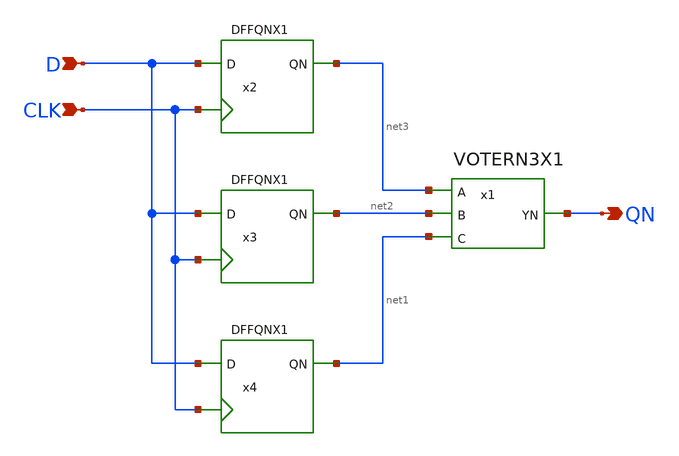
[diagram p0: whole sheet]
** sch_path: lib/xschem/TMRDFFQNX1.sch
**.subckt TMRDFFQNX1 D CLK QN
*.ipin D
*.ipin CLK
*.opin QN
x1 net3 net2 net1 QN VDD VSS VOTERN3X1
x2 CLK net3 D VDD VSS DFFQNX1
x3 CLK net2 D VDD VSS DFFQNX1
x4 CLK net1 D VDD VSS DFFQNX1
**.ends

* expanding   symbol:  VOTERN3X1.sym # of pins=4
** sym_path: VOTERN3X1.sym
** sch_path: VOTERN3X1.sch
.subckt VOTERN3X1 A B C YN VDD VSS
*.ipin A
*.opin YN
*.ipin B
*.ipin C
XM2 net1 A VDD VDD sky130_fd_pr__pfet_01v8 L=0.15 W=2 nf=1 ad='int((nf+1)/2) * W/nf * 0.29' as='int((nf+2)/2) * W/nf * 0.29'
+ pd='2*int((nf+1)/2) * (W/nf + 0.29)' ps='2*int((nf+2)/2) * (W/nf + 0.29)' nrd='0.29 / W' nrs='0.29 / W'
+ sa=0 sb=0 sd=0 mult=1 m=1
XM3 net2 B VSS VSS sky130_fd_pr__nfet_01v8 L=0.15 W=3 nf=1 ad='int((nf+1)/2) * W/nf * 0.29' as='int((nf+2)/2) * W/nf * 0.29'
+ pd='2*int((nf+1)/2) * (W/nf + 0.29)' ps='2*int((nf+2)/2) * (W/nf + 0.29)' nrd='0.29 / W' nrs='0.29 / W'
+ sa=0 sb=0 sd=0 mult=1 m=1
XM4 YN A net2 VSS sky130_fd_pr__nfet_01v8 L=0.15 W=3 nf=1 ad='int((nf+1)/2) * W/nf * 0.29' as='int((nf+2)/2) * W/nf * 0.29'
+ pd='2*int((nf+1)/2) * (W/nf + 0.29)' ps='2*int((nf+2)/2) * (W/nf + 0.29)' nrd='0.29 / W' nrs='0.29 / W'
+ sa=0 sb=0 sd=0 mult=1 m=1
XM5 net1 A VDD VDD sky130_fd_pr__pfet_01v8 L=0.15 W=2 nf=1 ad='int((nf+1)/2) * W/nf * 0.29' as='int((nf+2)/2) * W/nf * 0.29'
+ pd='2*int((nf+1)/2) * (W/nf + 0.29)' ps='2*int((nf+2)/2) * (W/nf + 0.29)' nrd='0.29 / W' nrs='0.29 / W'
+ sa=0 sb=0 sd=0 mult=1 m=1
XM6 net1 B VDD VDD sky130_fd_pr__pfet_01v8 L=0.15 W=2 nf=1 ad='int((nf+1)/2) * W/nf * 0.29' as='int((nf+2)/2) * W/nf * 0.29'
+ pd='2*int((nf+1)/2) * (W/nf + 0.29)' ps='2*int((nf+2)/2) * (W/nf + 0.29)' nrd='0.29 / W' nrs='0.29 / W'
+ sa=0 sb=0 sd=0 mult=1 m=1
XM7 net1 B VDD VDD sky130_fd_pr__pfet_01v8 L=0.15 W=2 nf=1 ad='int((nf+1)/2) * W/nf * 0.29' as='int((nf+2)/2) * W/nf * 0.29'
+ pd='2*int((nf+1)/2) * (W/nf + 0.29)' ps='2*int((nf+2)/2) * (W/nf + 0.29)' nrd='0.29 / W' nrs='0.29 / W'
+ sa=0 sb=0 sd=0 mult=1 m=1
XM10 net3 B net1 net1 sky130_fd_pr__pfet_01v8 L=0.15 W=2 nf=1 ad='int((nf+1)/2) * W/nf * 0.29' as='int((nf+2)/2) * W/nf * 0.29'
+ pd='2*int((nf+1)/2) * (W/nf + 0.29)' ps='2*int((nf+2)/2) * (W/nf + 0.29)' nrd='0.29 / W' nrs='0.29 / W'
+ sa=0 sb=0 sd=0 mult=1 m=1
XM11 net3 B net1 VDD sky130_fd_pr__pfet_01v8 L=0.15 W=2 nf=1 ad='int((nf+1)/2) * W/nf * 0.29' as='int((nf+2)/2) * W/nf * 0.29'
+ pd='2*int((nf+1)/2) * (W/nf + 0.29)' ps='2*int((nf+2)/2) * (W/nf + 0.29)' nrd='0.29 / W' nrs='0.29 / W'
+ sa=0 sb=0 sd=0 mult=1 m=1
XM12 YN C net3 net3 sky130_fd_pr__pfet_01v8 L=0.15 W=2 nf=1 ad='int((nf+1)/2) * W/nf * 0.29' as='int((nf+2)/2) * W/nf * 0.29'
+ pd='2*int((nf+1)/2) * (W/nf + 0.29)' ps='2*int((nf+2)/2) * (W/nf + 0.29)' nrd='0.29 / W' nrs='0.29 / W'
+ sa=0 sb=0 sd=0 mult=1 m=1
XM13 YN C net3 VDD sky130_fd_pr__pfet_01v8 L=0.15 W=2 nf=1 ad='int((nf+1)/2) * W/nf * 0.29' as='int((nf+2)/2) * W/nf * 0.29'
+ pd='2*int((nf+1)/2) * (W/nf + 0.29)' ps='2*int((nf+2)/2) * (W/nf + 0.29)' nrd='0.29 / W' nrs='0.29 / W'
+ sa=0 sb=0 sd=0 mult=1 m=1
XM14 net3 C net1 net1 sky130_fd_pr__pfet_01v8 L=0.15 W=2 nf=1 ad='int((nf+1)/2) * W/nf * 0.29' as='int((nf+2)/2) * W/nf * 0.29'
+ pd='2*int((nf+1)/2) * (W/nf + 0.29)' ps='2*int((nf+2)/2) * (W/nf + 0.29)' nrd='0.29 / W' nrs='0.29 / W'
+ sa=0 sb=0 sd=0 mult=1 m=1
XM15 net3 C net1 VDD sky130_fd_pr__pfet_01v8 L=0.15 W=2 nf=1 ad='int((nf+1)/2) * W/nf * 0.29' as='int((nf+2)/2) * W/nf * 0.29'
+ pd='2*int((nf+1)/2) * (W/nf + 0.29)' ps='2*int((nf+2)/2) * (W/nf + 0.29)' nrd='0.29 / W' nrs='0.29 / W'
+ sa=0 sb=0 sd=0 mult=1 m=1
XM16 YN A net3 net3 sky130_fd_pr__pfet_01v8 L=0.15 W=2 nf=1 ad='int((nf+1)/2) * W/nf * 0.29' as='int((nf+2)/2) * W/nf * 0.29'
+ pd='2*int((nf+1)/2) * (W/nf + 0.29)' ps='2*int((nf+2)/2) * (W/nf + 0.29)' nrd='0.29 / W' nrs='0.29 / W'
+ sa=0 sb=0 sd=0 mult=1 m=1
XM17 YN A net3 VDD sky130_fd_pr__pfet_01v8 L=0.15 W=2 nf=1 ad='int((nf+1)/2) * W/nf * 0.29' as='int((nf+2)/2) * W/nf * 0.29'
+ pd='2*int((nf+1)/2) * (W/nf + 0.29)' ps='2*int((nf+2)/2) * (W/nf + 0.29)' nrd='0.29 / W' nrs='0.29 / W'
+ sa=0 sb=0 sd=0 mult=1 m=1
XM8 net4 B VSS VSS sky130_fd_pr__nfet_01v8 L=0.15 W=3 nf=1 ad='int((nf+1)/2) * W/nf * 0.29' as='int((nf+2)/2) * W/nf * 0.29'
+ pd='2*int((nf+1)/2) * (W/nf + 0.29)' ps='2*int((nf+2)/2) * (W/nf + 0.29)' nrd='0.29 / W' nrs='0.29 / W'
+ sa=0 sb=0 sd=0 mult=1 m=1
XM9 YN C net4 VSS sky130_fd_pr__nfet_01v8 L=0.15 W=3 nf=1 ad='int((nf+1)/2) * W/nf * 0.29' as='int((nf+2)/2) * W/nf * 0.29'
+ pd='2*int((nf+1)/2) * (W/nf + 0.29)' ps='2*int((nf+2)/2) * (W/nf + 0.29)' nrd='0.29 / W' nrs='0.29 / W'
+ sa=0 sb=0 sd=0 mult=1 m=1
XM18 net5 C VSS VSS sky130_fd_pr__nfet_01v8 L=0.15 W=3 nf=1 ad='int((nf+1)/2) * W/nf * 0.29' as='int((nf+2)/2) * W/nf * 0.29'
+ pd='2*int((nf+1)/2) * (W/nf + 0.29)' ps='2*int((nf+2)/2) * (W/nf + 0.29)' nrd='0.29 / W' nrs='0.29 / W'
+ sa=0 sb=0 sd=0 mult=1 m=1
XM19 YN A net5 VSS sky130_fd_pr__nfet_01v8 L=0.15 W=3 nf=1 ad='int((nf+1)/2) * W/nf * 0.29' as='int((nf+2)/2) * W/nf * 0.29'
+ pd='2*int((nf+1)/2) * (W/nf + 0.29)' ps='2*int((nf+2)/2) * (W/nf + 0.29)' nrd='0.29 / W' nrs='0.29 / W'
+ sa=0 sb=0 sd=0 mult=1 m=1
.ends


* expanding   symbol:  DFFQNX1.sym # of pins=3
** sym_path: DFFQNX1.sym
** sch_path: DFFQNX1.sch
.subckt DFFQNX1 CLK QN D VDD VSS
*.ipin CLK
*.ipin D
*.opin QN
x1 B1 C1 CLK A1 NAND3X1
x2 A1 B1 D NAND2X1
x3 D1 A1 C1 NAND2X1
x4 C1 D1 CLK NAND2X1
x5 QN B1 net1 NAND2X1
x6 net1 QN C1 NAND2X1
.ends


* expanding   symbol:  NAND3X1.sym # of pins=4
** sym_path: lib/xschem/NAND3X1.sym
** sch_path: lib/xschem/NAND3X1.sch
.subckt NAND3X1 Y A B C
*.ipin A
*.opin Y
*.ipin B
*.ipin C
XM1 net2 C GND GND sky130_fd_pr__nfet_01v8 L=0.15 W=3 nf=1 ad='int((nf+1)/2) * W/nf * 0.29' as='int((nf+2)/2) * W/nf * 0.29'
+ pd='2*int((nf+1)/2) * (W/nf + 0.29)' ps='2*int((nf+2)/2) * (W/nf + 0.29)' nrd='0.29 / W' nrs='0.29 / W'
+ sa=0 sb=0 sd=0 mult=1 m=1
XM2 Y A VDD VDD sky130_fd_pr__pfet_01v8 L=0.15 W=2 nf=1 ad='int((nf+1)/2) * W/nf * 0.29' as='int((nf+2)/2) * W/nf * 0.29'
+ pd='2*int((nf+1)/2) * (W/nf + 0.29)' ps='2*int((nf+2)/2) * (W/nf + 0.29)' nrd='0.29 / W' nrs='0.29 / W'
+ sa=0 sb=0 sd=0 mult=1 m=1
XM3 net1 B net2 GND sky130_fd_pr__nfet_01v8 L=0.15 W=3 nf=1 ad='int((nf+1)/2) * W/nf * 0.29' as='int((nf+2)/2) * W/nf * 0.29'
+ pd='2*int((nf+1)/2) * (W/nf + 0.29)' ps='2*int((nf+2)/2) * (W/nf + 0.29)' nrd='0.29 / W' nrs='0.29 / W'
+ sa=0 sb=0 sd=0 mult=1 m=1
XM4 Y A net1 GND sky130_fd_pr__nfet_01v8 L=0.15 W=3 nf=1 ad='int((nf+1)/2) * W/nf * 0.29' as='int((nf+2)/2) * W/nf * 0.29'
+ pd='2*int((nf+1)/2) * (W/nf + 0.29)' ps='2*int((nf+2)/2) * (W/nf + 0.29)' nrd='0.29 / W' nrs='0.29 / W'
+ sa=0 sb=0 sd=0 mult=1 m=1
XM5 Y A VDD VDD sky130_fd_pr__pfet_01v8 L=0.15 W=2 nf=1 ad='int((nf+1)/2) * W/nf * 0.29' as='int((nf+2)/2) * W/nf * 0.29'
+ pd='2*int((nf+1)/2) * (W/nf + 0.29)' ps='2*int((nf+2)/2) * (W/nf + 0.29)' nrd='0.29 / W' nrs='0.29 / W'
+ sa=0 sb=0 sd=0 mult=1 m=1
XM6 Y B VDD VDD sky130_fd_pr__pfet_01v8 L=0.15 W=2 nf=1 ad='int((nf+1)/2) * W/nf * 0.29' as='int((nf+2)/2) * W/nf * 0.29'
+ pd='2*int((nf+1)/2) * (W/nf + 0.29)' ps='2*int((nf+2)/2) * (W/nf + 0.29)' nrd='0.29 / W' nrs='0.29 / W'
+ sa=0 sb=0 sd=0 mult=1 m=1
XM7 Y B VDD VDD sky130_fd_pr__pfet_01v8 L=0.15 W=2 nf=1 ad='int((nf+1)/2) * W/nf * 0.29' as='int((nf+2)/2) * W/nf * 0.29'
+ pd='2*int((nf+1)/2) * (W/nf + 0.29)' ps='2*int((nf+2)/2) * (W/nf + 0.29)' nrd='0.29 / W' nrs='0.29 / W'
+ sa=0 sb=0 sd=0 mult=1 m=1
XM8 Y C VDD VDD sky130_fd_pr__pfet_01v8 L=0.15 W=2 nf=1 ad='int((nf+1)/2) * W/nf * 0.29' as='int((nf+2)/2) * W/nf * 0.29'
+ pd='2*int((nf+1)/2) * (W/nf + 0.29)' ps='2*int((nf+2)/2) * (W/nf + 0.29)' nrd='0.29 / W' nrs='0.29 / W'
+ sa=0 sb=0 sd=0 mult=1 m=1
XM9 Y C VDD VDD sky130_fd_pr__pfet_01v8 L=0.15 W=2 nf=1 ad='int((nf+1)/2) * W/nf * 0.29' as='int((nf+2)/2) * W/nf * 0.29'
+ pd='2*int((nf+1)/2) * (W/nf + 0.29)' ps='2*int((nf+2)/2) * (W/nf + 0.29)' nrd='0.29 / W' nrs='0.29 / W'
+ sa=0 sb=0 sd=0 mult=1 m=1
.ends


* expanding   symbol:  NAND2X1.sym # of pins=3
** sym_path: lib/xschem/NAND2X1.sym
** sch_path: lib/xschem/NAND2X1.sch
.subckt NAND2X1 Y A B
*.ipin A
*.opin Y
*.ipin B
XM1 Y A VDD VDD sky130_fd_pr__pfet_01v8 L=0.15 W=2 nf=1 ad='int((nf+1)/2) * W/nf * 0.29' as='int((nf+2)/2) * W/nf * 0.29'
+ pd='2*int((nf+1)/2) * (W/nf + 0.29)' ps='2*int((nf+2)/2) * (W/nf + 0.29)' nrd='0.29 / W' nrs='0.29 / W'
+ sa=0 sb=0 sd=0 mult=1 m=1
XM5 Y A net1 VSS sky130_fd_pr__nfet_01v8 L=0.15 W=3 nf=1 ad='int((nf+1)/2) * W/nf * 0.29' as='int((nf+2)/2) * W/nf * 0.29'
+ pd='2*int((nf+1)/2) * (W/nf + 0.29)' ps='2*int((nf+2)/2) * (W/nf + 0.29)' nrd='0.29 / W' nrs='0.29 / W'
+ sa=0 sb=0 sd=0 mult=1 m=1
XM2 Y A VDD VDD sky130_fd_pr__pfet_01v8 L=0.15 W=2 nf=1 ad='int((nf+1)/2) * W/nf * 0.29' as='int((nf+2)/2) * W/nf * 0.29'
+ pd='2*int((nf+1)/2) * (W/nf + 0.29)' ps='2*int((nf+2)/2) * (W/nf + 0.29)' nrd='0.29 / W' nrs='0.29 / W'
+ sa=0 sb=0 sd=0 mult=1 m=1
XM3 Y B VDD VDD sky130_fd_pr__pfet_01v8 L=0.15 W=2 nf=1 ad='int((nf+1)/2) * W/nf * 0.29' as='int((nf+2)/2) * W/nf * 0.29'
+ pd='2*int((nf+1)/2) * (W/nf + 0.29)' ps='2*int((nf+2)/2) * (W/nf + 0.29)' nrd='0.29 / W' nrs='0.29 / W'
+ sa=0 sb=0 sd=0 mult=1 m=1
XM4 Y B VDD VDD sky130_fd_pr__pfet_01v8 L=0.15 W=2 nf=1 ad='int((nf+1)/2) * W/nf * 0.29' as='int((nf+2)/2) * W/nf * 0.29'
+ pd='2*int((nf+1)/2) * (W/nf + 0.29)' ps='2*int((nf+2)/2) * (W/nf + 0.29)' nrd='0.29 / W' nrs='0.29 / W'
+ sa=0 sb=0 sd=0 mult=1 m=1
XM6 net1 B VSS VSS sky130_fd_pr__nfet_01v8 L=0.15 W=3 nf=1 ad='int((nf+1)/2) * W/nf * 0.29' as='int((nf+2)/2) * W/nf * 0.29'
+ pd='2*int((nf+1)/2) * (W/nf + 0.29)' ps='2*int((nf+2)/2) * (W/nf + 0.29)' nrd='0.29 / W' nrs='0.29 / W'
+ sa=0 sb=0 sd=0 mult=1 m=1
.ends

.GLOBAL VDD
.GLOBAL GND
.end
